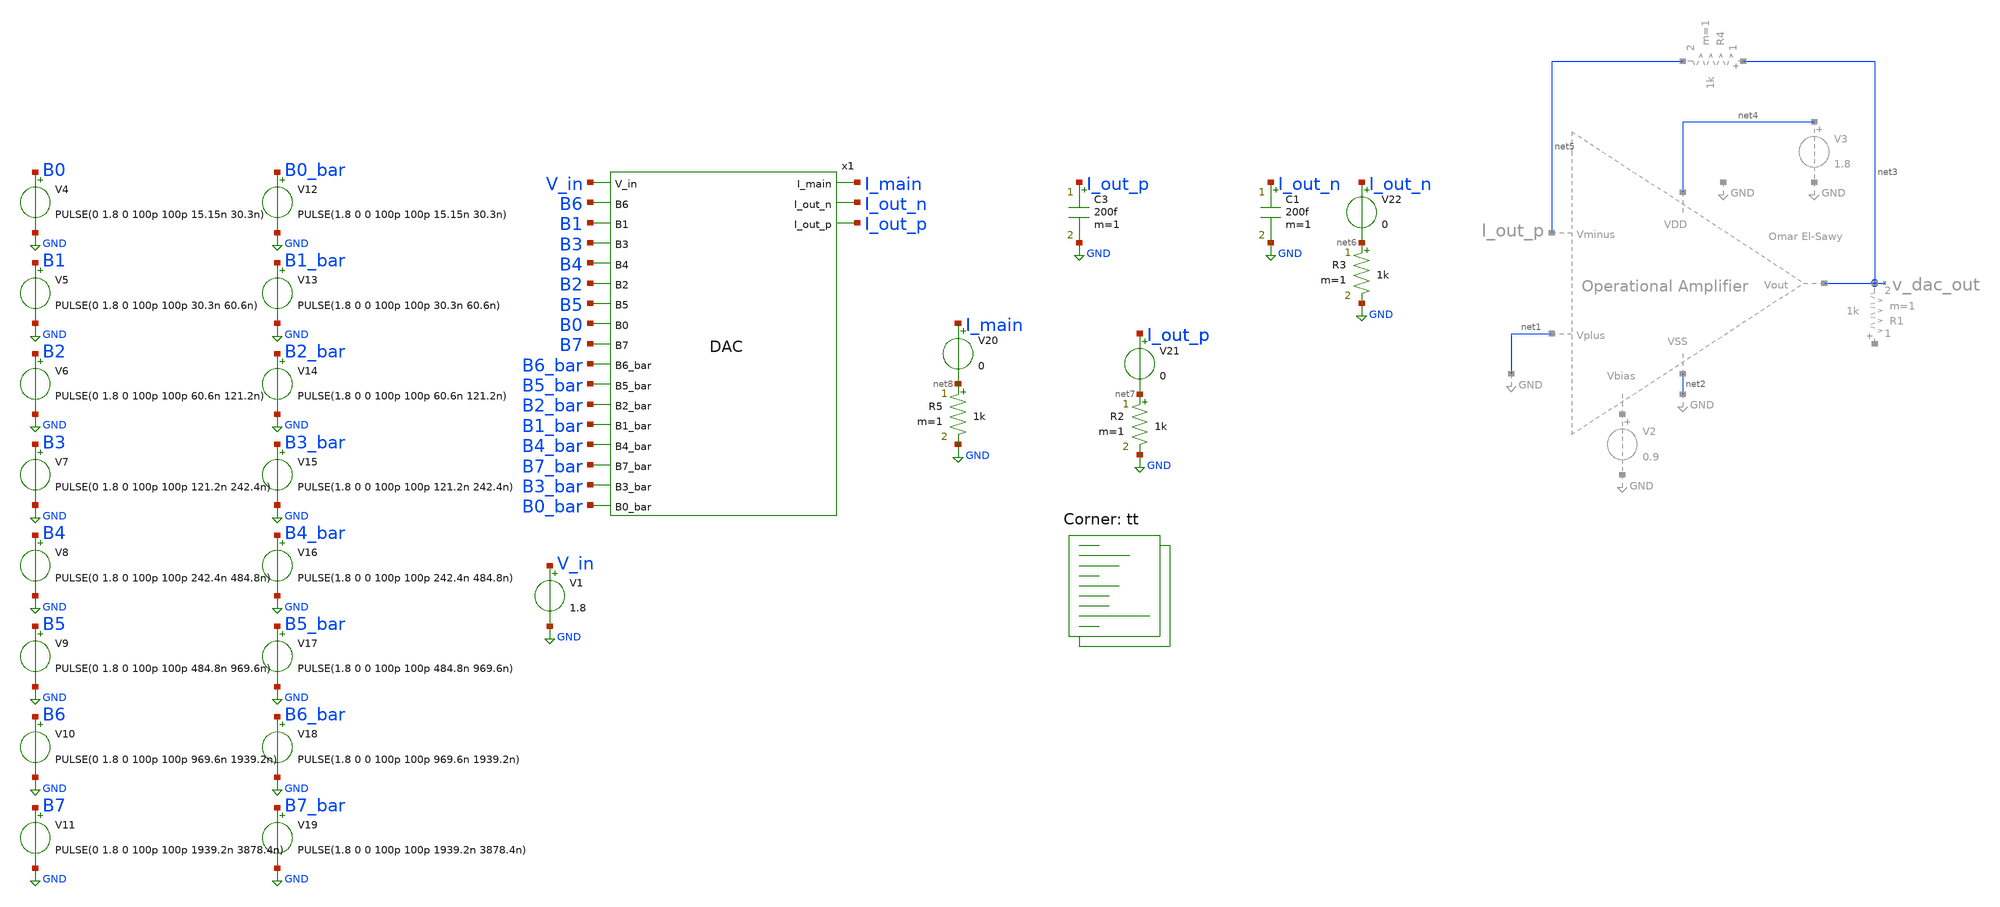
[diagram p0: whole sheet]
** sch_path: analog/library/DAC/Custom/testbenches/DAC_tb.sch
**.subckt DAC_tb
x1 V_in I_main I_out_n I_out_p B6 B1 B3 B4 B2 B5 B0 B7 B6_bar B5_bar B2_bar B1_bar B4_bar B7_bar
+ B3_bar B0_bar DAC
V4 B0 GND PULSE(0 1.8 0 100p 100p 15.15n 30.3n)
V5 B1 GND PULSE(0 1.8 0 100p 100p 30.3n 60.6n)
V6 B2 GND PULSE(0 1.8 0 100p 100p 60.6n 121.2n)
V7 B3 GND PULSE(0 1.8 0 100p 100p 121.2n 242.4n)
V8 B4 GND PULSE(0 1.8 0 100p 100p 242.4n 484.8n)
V9 B5 GND PULSE(0 1.8 0 100p 100p 484.8n 969.6n)
V10 B6 GND PULSE(0 1.8 0 100p 100p 969.6n 1939.2n)
V11 B7 GND PULSE(0 1.8 0 100p 100p 1939.2n 3878.4n)
V12 B0_bar GND PULSE(1.8 0 0 100p 100p 15.15n 30.3n)
V13 B1_bar GND PULSE(1.8 0 0 100p 100p 30.3n 60.6n)
V14 B2_bar GND PULSE(1.8 0 0 100p 100p 60.6n 121.2n)
V15 B3_bar GND PULSE(1.8 0 0 100p 100p 121.2n 242.4n)
V16 B4_bar GND PULSE(1.8 0 0 100p 100p 242.4n 484.8n)
V17 B5_bar GND PULSE(1.8 0 0 100p 100p 484.8n 969.6n)
V18 B6_bar GND PULSE(1.8 0 0 100p 100p 969.6n 1939.2n)
V19 B7_bar GND PULSE(1.8 0 0 100p 100p 1939.2n 3878.4n)
V1 V_in GND 1.8
C3 I_out_p GND 200f m=1
C1 I_out_n GND 200f m=1
V22 I_out_n net6 0
R3 net6 GND 1k m=1
V21 I_out_p net7 0
R2 net7 GND 1k m=1
V20 I_main net8 0
R5 net8 GND 1k m=1
**** begin user architecture code
.lib $::SKYWATER_MODELS/sky130.lib.spice tt

.control
* Longer simulation with slower switching
tran 100p 3878.4n
* Plot differential output
let diff_out = v(I_out_p) - v(I_out_n)
plot diff_out

* Also plot individual outputs to see if one is noisier
plot v(I_out_p) v(I_out_n)

write DAC_tb.raw
.endc

.end

**** end user architecture code
**.ends
.GLOBAL GND
.end
